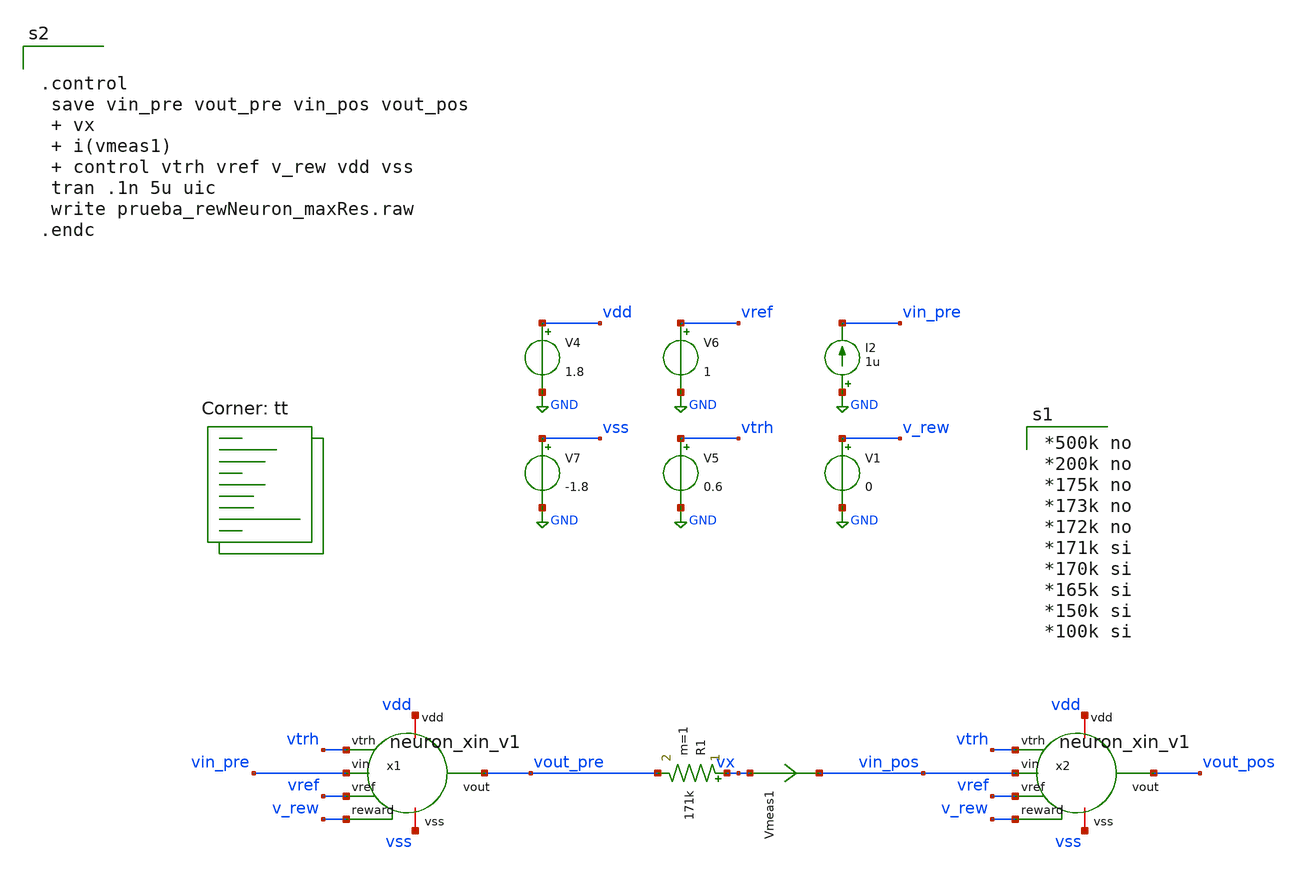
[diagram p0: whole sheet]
** sch_path: designs/tb_xin_neuron_v1/prueba_rewNeuron_maxRes.sch
**.subckt prueba_rewNeuron_maxRes
V4 vdd GND 1.8
V5 vtrh GND 0.6
V6 vref GND 1
V7 vss GND -1.8
V1 v_rew GND 0
Vmeas1 vx vin_pos 0
.save i(vmeas1)
I2 GND vin_pre 1u
R1 vx vout_pre 171k m=1
x1 vdd vss vout_pre vin_pre vtrh vref v_rew neuron_xin_v1
x2 vdd vss vout_pos vin_pos vtrh vref v_rew neuron_xin_v1
**** begin user architecture code


.control
 save vin_pre vout_pre vin_pos vout_pos
 + vx
 + i(vmeas1)
 + control vtrh vref v_rew vdd vss
 tran .1n 5u uic
 write prueba_rewNeuron_maxRes.raw
.endc




*500k no
*200k no
*175k no
*173k no
*172k no
*171k si
*170k si
*165k si
*150k si
*100k si

.lib $::SKYWATER_MODELS/sky130.lib.spice tt
**** end user architecture code
**.ends
.GLOBAL GND
.end
